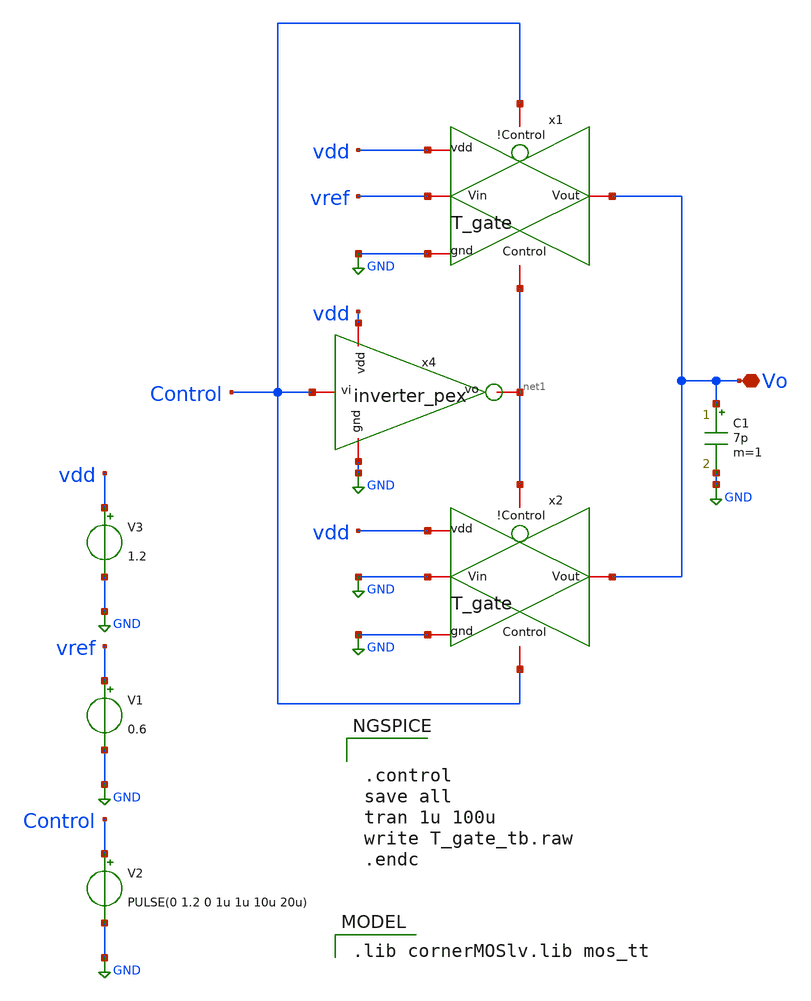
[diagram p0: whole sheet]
** sch_path: xschem/T_gate_switch_tb_ps.sch
**.subckt T_gate_switch_tb_ps Vo
*.iopin Vo
V1 vref GND 0.6
V2 Control GND PULSE(0 1.2 0 1u 1u 10u 20u)
V3 vdd GND 1.2
C1 Vo GND 7p m=1
x4 vdd Control net1 GND inverter_pex
x1 Control vref Vo GND net1 vdd T_gate
x2 net1 GND Vo GND Control vdd T_gate
**** begin user architecture code


.control
save all
tran 1u 100u
write T_gate_tb.raw
.endc


 .lib cornerMOSlv.lib mos_tt

**** end user architecture code
**.ends

* expanding   symbol:
*+  /home/userdata/k67D/duynk_67d/SAR_ADC_8BIT_IHP/pex/xschem_pex_symbol/inverter_pex.sym # of pins=4
** sym_path: /home/userdata/k67D/duynk_67d/SAR_ADC_8BIT_IHP/pex/xschem_pex_symbol/inverter.sym

.subckt inverter_pex vdd vi vo gnd
X0 vo.t0 vi.t0 vdd.t1 vdd.t0 sg13_lv_pmos ad=0.272p pd=2.28u as=0.272p ps=2.28u w=0.8u l=0.13u
X1 vo.t1 vi.t0 gnd.t1 gnd.t0 sg13_lv_nmos ad=0.136p pd=1.48u as=0.136p ps=1.48u w=0.4u l=0.13u
C0 vdd vi 0.09004f
C1 vdd vo 0.12375f
C2 vi vo 0.06195f
R0 vi vi.t0 15.0294
R1 vdd.n0 vdd.t0 11.3708
R2 vdd.n0 vdd.t1 8.93718
R3 vdd vdd.n0 0.0808279
R4 vo.n0 vo.t1 17.2852
R5 vo.n0 vo.t0 9.11151
R6 vo vo.n0 0.19025
R7 gnd.n0 gnd.t0 1381.52
R8 gnd.n0 gnd.t1 17.3745
R9 gnd gnd.n0 0.079713
C3 vo gnd 0.20432f
C4 vi gnd 0.35463f
C5 vdd gnd 0.1104f
.ends


* expanding   symbol:
*+  /home/userdata/k67D/duynk_67d/SAR_ADC_8BIT_IHP/pex/xschem_pex_symbol/T_gate.sym # of pins=6
** sym_path: /home/userdata/k67D/duynk_67d/SAR_ADC_8BIT_IHP/pex/xschem_pex_symbol/T_gate.sym

.subckt T_gate Vin Vout Control gnd vdd
X0 Vout.t1 Control.t0 Vin.t1 gnd.t0 sg13_lv_nmos ad=0.34p pd=2.68u as=0.34p ps=2.68u w=1u l=0.13u
X1 Vout.t0 Control.t0 Vin.t0 vdd.t0 sg13_lv_pmos ad=0.68p pd=4.68u as=0.68p ps=4.68u w=2u l=0.13u
C0 Control Vin 0.01009f
C1 Control vdd 0.06532f
C2 Vin Vout 0.44023f
C3 Vin vdd 0.01888f
C4 Vout vdd 0.19552f
R0 Control Control.t0 15.0225
R1 Vin.n0 Vin.t1 6.32304
R2 Vin.n0 Vin.t0 3.74651
R3 Vin Vin.n0 0.255378
R4 Vout.n0 Vout.t1 6.32648
R5 Vout.n0 Vout.t0 3.74651
R6 Vout Vout.n0 0.71275
R7 gnd gnd.t0 810.898
R8 Control Control.t0 15.0243
R9 vdd vdd.n0 17.0173
R10 vdd vdd.n0 5.79683
R11 vdd.n0 vdd.t0 4.25112
C5 Control gnd 0.26277f
C6 Vout gnd 0.30897f
C7 Vin gnd 0.22881f
C8 Control gnd 0.30202f
C9 vdd gnd 0.09029f
.ends

.GLOBAL GND
.end
